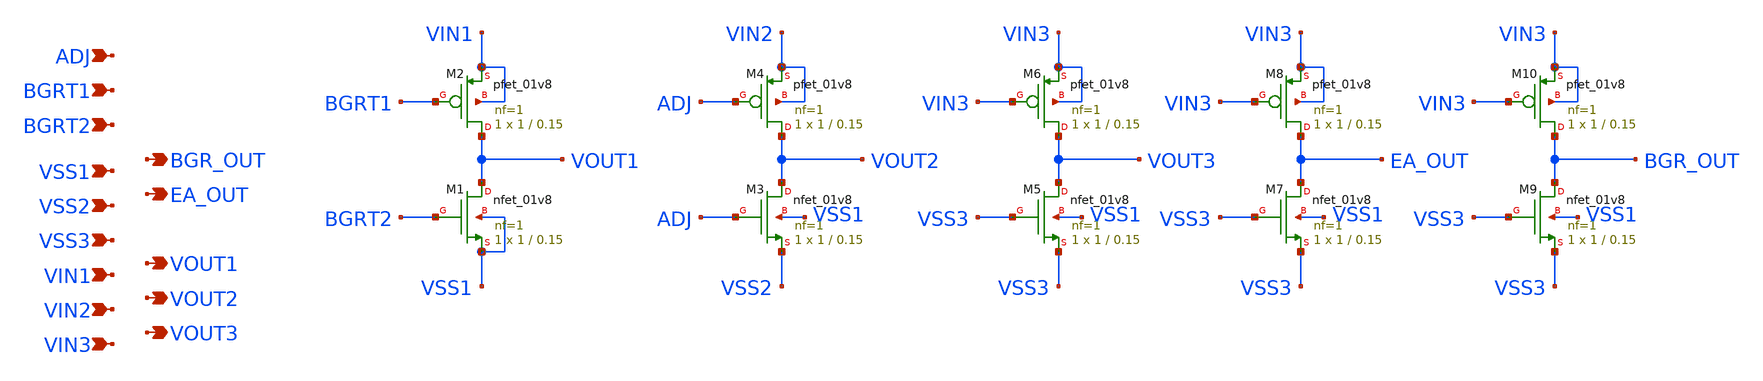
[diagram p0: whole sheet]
** sch_path: xschem/ulqc_ldo.sch
**.subckt ulqc_ldo VSS1 VIN1 VIN2 VIN3 ADJ BGRT1 BGRT2 BGR_OUT EA_OUT VOUT1 VOUT2 VOUT3 VSS2 VSS3
*.ipin VSS1
*.ipin VIN1
*.ipin VIN2
*.ipin VIN3
*.ipin ADJ
*.ipin BGRT1
*.ipin BGRT2
*.opin BGR_OUT
*.opin EA_OUT
*.opin VOUT1
*.opin VOUT2
*.opin VOUT3
*.ipin VSS2
*.ipin VSS3
XM1 VOUT1 BGRT2 VSS1 VSS1 sky130_fd_pr__nfet_01v8 L=0.15 W=1 nf=1 ad='int((nf+1)/2) * W/nf * 0.29' as='int((nf+2)/2) * W/nf * 0.29'
+ pd='2*int((nf+1)/2) * (W/nf + 0.29)' ps='2*int((nf+2)/2) * (W/nf + 0.29)' nrd='0.29 / W' nrs='0.29 / W'
+ sa=0 sb=0 sd=0 mult=1 m=1
XM2 VOUT1 BGRT1 VIN1 VIN1 sky130_fd_pr__pfet_01v8 L=0.15 W=1 nf=1 ad='int((nf+1)/2) * W/nf * 0.29' as='int((nf+2)/2) * W/nf * 0.29'
+ pd='2*int((nf+1)/2) * (W/nf + 0.29)' ps='2*int((nf+2)/2) * (W/nf + 0.29)' nrd='0.29 / W' nrs='0.29 / W'
+ sa=0 sb=0 sd=0 mult=1 m=1
XM3 VOUT2 ADJ VSS2 VSS1 sky130_fd_pr__nfet_01v8 L=0.15 W=1 nf=1 ad='int((nf+1)/2) * W/nf * 0.29' as='int((nf+2)/2) * W/nf * 0.29'
+ pd='2*int((nf+1)/2) * (W/nf + 0.29)' ps='2*int((nf+2)/2) * (W/nf + 0.29)' nrd='0.29 / W' nrs='0.29 / W'
+ sa=0 sb=0 sd=0 mult=1 m=1
XM4 VOUT2 ADJ VIN2 VIN2 sky130_fd_pr__pfet_01v8 L=0.15 W=1 nf=1 ad='int((nf+1)/2) * W/nf * 0.29' as='int((nf+2)/2) * W/nf * 0.29'
+ pd='2*int((nf+1)/2) * (W/nf + 0.29)' ps='2*int((nf+2)/2) * (W/nf + 0.29)' nrd='0.29 / W' nrs='0.29 / W'
+ sa=0 sb=0 sd=0 mult=1 m=1
XM5 VOUT3 VSS3 VSS3 VSS1 sky130_fd_pr__nfet_01v8 L=0.15 W=1 nf=1 ad='int((nf+1)/2) * W/nf * 0.29' as='int((nf+2)/2) * W/nf * 0.29'
+ pd='2*int((nf+1)/2) * (W/nf + 0.29)' ps='2*int((nf+2)/2) * (W/nf + 0.29)' nrd='0.29 / W' nrs='0.29 / W'
+ sa=0 sb=0 sd=0 mult=1 m=1
XM6 VOUT3 VIN3 VIN3 VIN3 sky130_fd_pr__pfet_01v8 L=0.15 W=1 nf=1 ad='int((nf+1)/2) * W/nf * 0.29' as='int((nf+2)/2) * W/nf * 0.29'
+ pd='2*int((nf+1)/2) * (W/nf + 0.29)' ps='2*int((nf+2)/2) * (W/nf + 0.29)' nrd='0.29 / W' nrs='0.29 / W'
+ sa=0 sb=0 sd=0 mult=1 m=1
XM7 EA_OUT VSS3 VSS3 VSS1 sky130_fd_pr__nfet_01v8 L=0.15 W=1 nf=1 ad='int((nf+1)/2) * W/nf * 0.29' as='int((nf+2)/2) * W/nf * 0.29'
+ pd='2*int((nf+1)/2) * (W/nf + 0.29)' ps='2*int((nf+2)/2) * (W/nf + 0.29)' nrd='0.29 / W' nrs='0.29 / W'
+ sa=0 sb=0 sd=0 mult=1 m=1
XM8 EA_OUT VIN3 VIN3 VIN3 sky130_fd_pr__pfet_01v8 L=0.15 W=1 nf=1 ad='int((nf+1)/2) * W/nf * 0.29' as='int((nf+2)/2) * W/nf * 0.29'
+ pd='2*int((nf+1)/2) * (W/nf + 0.29)' ps='2*int((nf+2)/2) * (W/nf + 0.29)' nrd='0.29 / W' nrs='0.29 / W'
+ sa=0 sb=0 sd=0 mult=1 m=1
XM9 BGR_OUT VSS3 VSS3 VSS1 sky130_fd_pr__nfet_01v8 L=0.15 W=1 nf=1 ad='int((nf+1)/2) * W/nf * 0.29' as='int((nf+2)/2) * W/nf * 0.29'
+ pd='2*int((nf+1)/2) * (W/nf + 0.29)' ps='2*int((nf+2)/2) * (W/nf + 0.29)' nrd='0.29 / W' nrs='0.29 / W'
+ sa=0 sb=0 sd=0 mult=1 m=1
XM10 BGR_OUT VIN3 VIN3 VIN3 sky130_fd_pr__pfet_01v8 L=0.15 W=1 nf=1 ad='int((nf+1)/2) * W/nf * 0.29'
+ as='int((nf+2)/2) * W/nf * 0.29' pd='2*int((nf+1)/2) * (W/nf + 0.29)' ps='2*int((nf+2)/2) * (W/nf + 0.29)'
+ nrd='0.29 / W' nrs='0.29 / W' sa=0 sb=0 sd=0 mult=1 m=1
**.ends
.end
